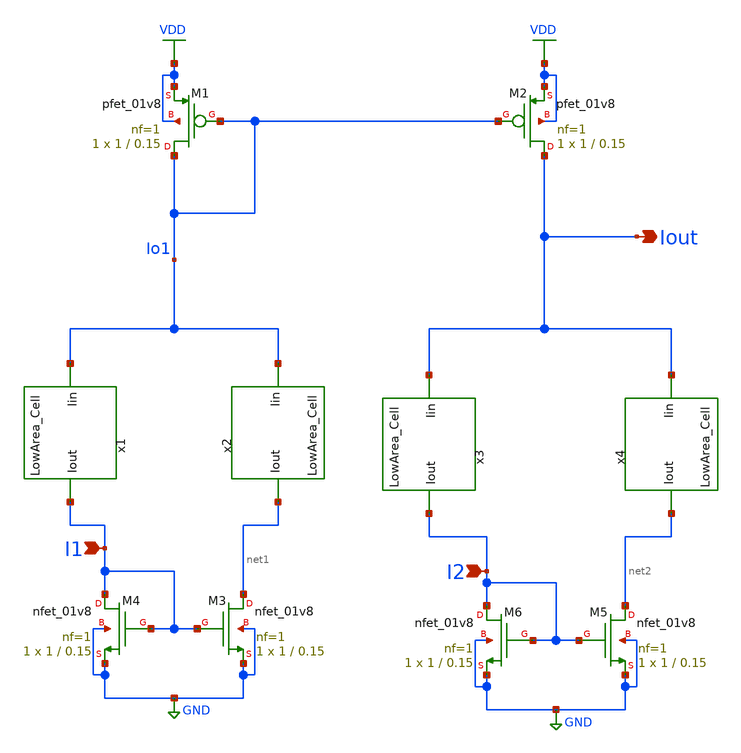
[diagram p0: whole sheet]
** sch_path: analog/schematics/components/CurrentMutltiplier/CurrentMultiplier_LowArea.sch
**.subckt CurrentMultiplier_LowArea Iout I1 I2
*.opin Iout
*.ipin I1
*.ipin I2
x1 I1 Io1 LowArea_Cell
x2 net1 Io1 LowArea_Cell
x3 I2 Iout LowArea_Cell
x4 net2 Iout LowArea_Cell
XM1 Io1 Io1 VDD VDD sky130_fd_pr__pfet_01v8 L=0.15 W=1 nf=1 ad='int((nf+1)/2) * W/nf * 0.29' as='int((nf+2)/2) * W/nf * 0.29'
+ pd='2*int((nf+1)/2) * (W/nf + 0.29)' ps='2*int((nf+2)/2) * (W/nf + 0.29)' nrd='0.29 / W' nrs='0.29 / W'
+ sa=0 sb=0 sd=0 mult=1 m=1
XM2 Iout Io1 VDD VDD sky130_fd_pr__pfet_01v8 L=0.15 W=1 nf=1 ad='int((nf+1)/2) * W/nf * 0.29' as='int((nf+2)/2) * W/nf * 0.29'
+ pd='2*int((nf+1)/2) * (W/nf + 0.29)' ps='2*int((nf+2)/2) * (W/nf + 0.29)' nrd='0.29 / W' nrs='0.29 / W'
+ sa=0 sb=0 sd=0 mult=1 m=1
XM3 net1 I1 GND GND sky130_fd_pr__nfet_01v8 L=0.15 W=1 nf=1 ad='int((nf+1)/2) * W/nf * 0.29' as='int((nf+2)/2) * W/nf * 0.29'
+ pd='2*int((nf+1)/2) * (W/nf + 0.29)' ps='2*int((nf+2)/2) * (W/nf + 0.29)' nrd='0.29 / W' nrs='0.29 / W'
+ sa=0 sb=0 sd=0 mult=1 m=1
XM4 I1 I1 GND GND sky130_fd_pr__nfet_01v8 L=0.15 W=1 nf=1 ad='int((nf+1)/2) * W/nf * 0.29' as='int((nf+2)/2) * W/nf * 0.29'
+ pd='2*int((nf+1)/2) * (W/nf + 0.29)' ps='2*int((nf+2)/2) * (W/nf + 0.29)' nrd='0.29 / W' nrs='0.29 / W'
+ sa=0 sb=0 sd=0 mult=1 m=1
XM5 net2 I2 GND GND sky130_fd_pr__nfet_01v8 L=0.15 W=1 nf=1 ad='int((nf+1)/2) * W/nf * 0.29' as='int((nf+2)/2) * W/nf * 0.29'
+ pd='2*int((nf+1)/2) * (W/nf + 0.29)' ps='2*int((nf+2)/2) * (W/nf + 0.29)' nrd='0.29 / W' nrs='0.29 / W'
+ sa=0 sb=0 sd=0 mult=1 m=1
XM6 I2 I2 GND GND sky130_fd_pr__nfet_01v8 L=0.15 W=1 nf=1 ad='int((nf+1)/2) * W/nf * 0.29' as='int((nf+2)/2) * W/nf * 0.29'
+ pd='2*int((nf+1)/2) * (W/nf + 0.29)' ps='2*int((nf+2)/2) * (W/nf + 0.29)' nrd='0.29 / W' nrs='0.29 / W'
+ sa=0 sb=0 sd=0 mult=1 m=1
**.ends

* expanding   symbol:  CurrentMultiplier/LowArea_Cell.sym # of pins=2
** sym_path: analog/schematics/components/LowAreaCell/LowArea_Cell.sym
** sch_path: analog/schematics/components/LowAreaCell/LowArea_Cell.sch
.subckt LowArea_Cell Iout Iin
*.ipin Iin
*.opin Iout
XM1 Iout Iin VSS GND sky130_fd_pr__nfet_01v8_lvt L=0.15 W=1 nf=1 ad='int((nf+1)/2) * W/nf * 0.29' as='int((nf+2)/2) * W/nf * 0.29'
+ pd='2*int((nf+1)/2) * (W/nf + 0.29)' ps='2*int((nf+2)/2) * (W/nf + 0.29)' nrd='0.29 / W' nrs='0.29 / W'
+ sa=0 sb=0 sd=0 mult=1 m=1
XR1 GND Iin GND sky130_fd_pr__res_high_po_5p73 L=11 mult=1 m=1
.ends

.GLOBAL VDD
.GLOBAL GND
.GLOBAL VSS
.end
